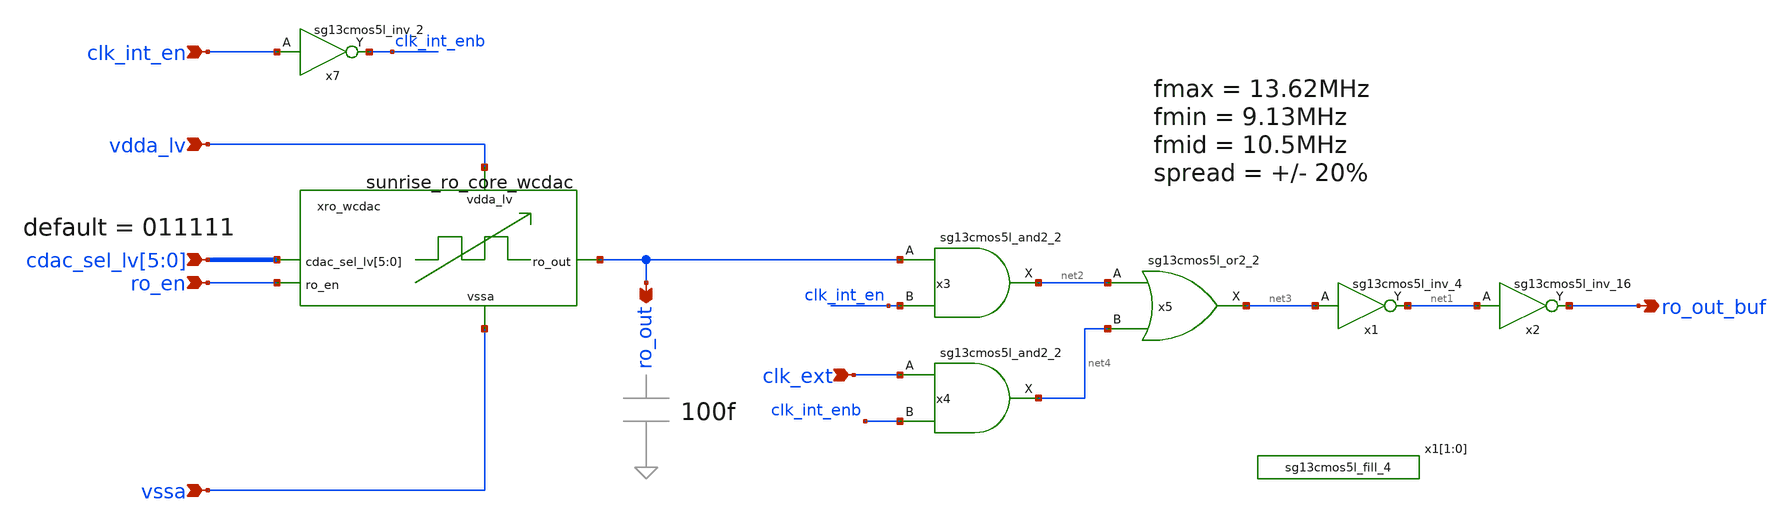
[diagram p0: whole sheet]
** sch_path: Schematics_Layout/sunrise_ro_core_wcdac_buf/sunrise_ro_core_wcdac_buf.sch
**.subckt sunrise_ro_core_wcdac_buf vdda_lv vssa ro_en
*+ cdac_sel_lv[5],cdac_sel_lv[4],cdac_sel_lv[3],cdac_sel_lv[2],cdac_sel_lv[1],cdac_sel_lv[0] ro_out_buf ro_out clk_ext clk_int_en
*.ipin vdda_lv
*.ipin vssa
*.ipin ro_en
*.ipin cdac_sel_lv[5],cdac_sel_lv[4],cdac_sel_lv[3],cdac_sel_lv[2],cdac_sel_lv[1],cdac_sel_lv[0]
*.opin ro_out_buf
*.opin ro_out
*.ipin clk_ext
*.ipin clk_int_en
xro_wcdac vdda_lv ro_out ro_en cdac_sel_lv[5] cdac_sel_lv[4] cdac_sel_lv[3] cdac_sel_lv[2]
+ cdac_sel_lv[1] cdac_sel_lv[0] vssa sunrise_ro_core_wcdac
x2 ro_out_buf net1 vdda_lv vssa sg13cmos5l_inv_16
x1 net1 net3 vdda_lv vssa sg13cmos5l_inv_4
x3 net2 ro_out clk_int_en vdda_lv vssa sg13cmos5l_and2_2
x4 net4 clk_ext clk_int_enb vdda_lv vssa sg13cmos5l_and2_2
x5 net3 net2 net4 vdda_lv vssa sg13cmos5l_or2_2
x7 clk_int_enb clk_int_en vdda_lv vssa sg13cmos5l_inv_2
x1[1] VDD VSS sg13cmos5l_fill_4
x1[0] VDD VSS sg13cmos5l_fill_4
**.ends
.end
